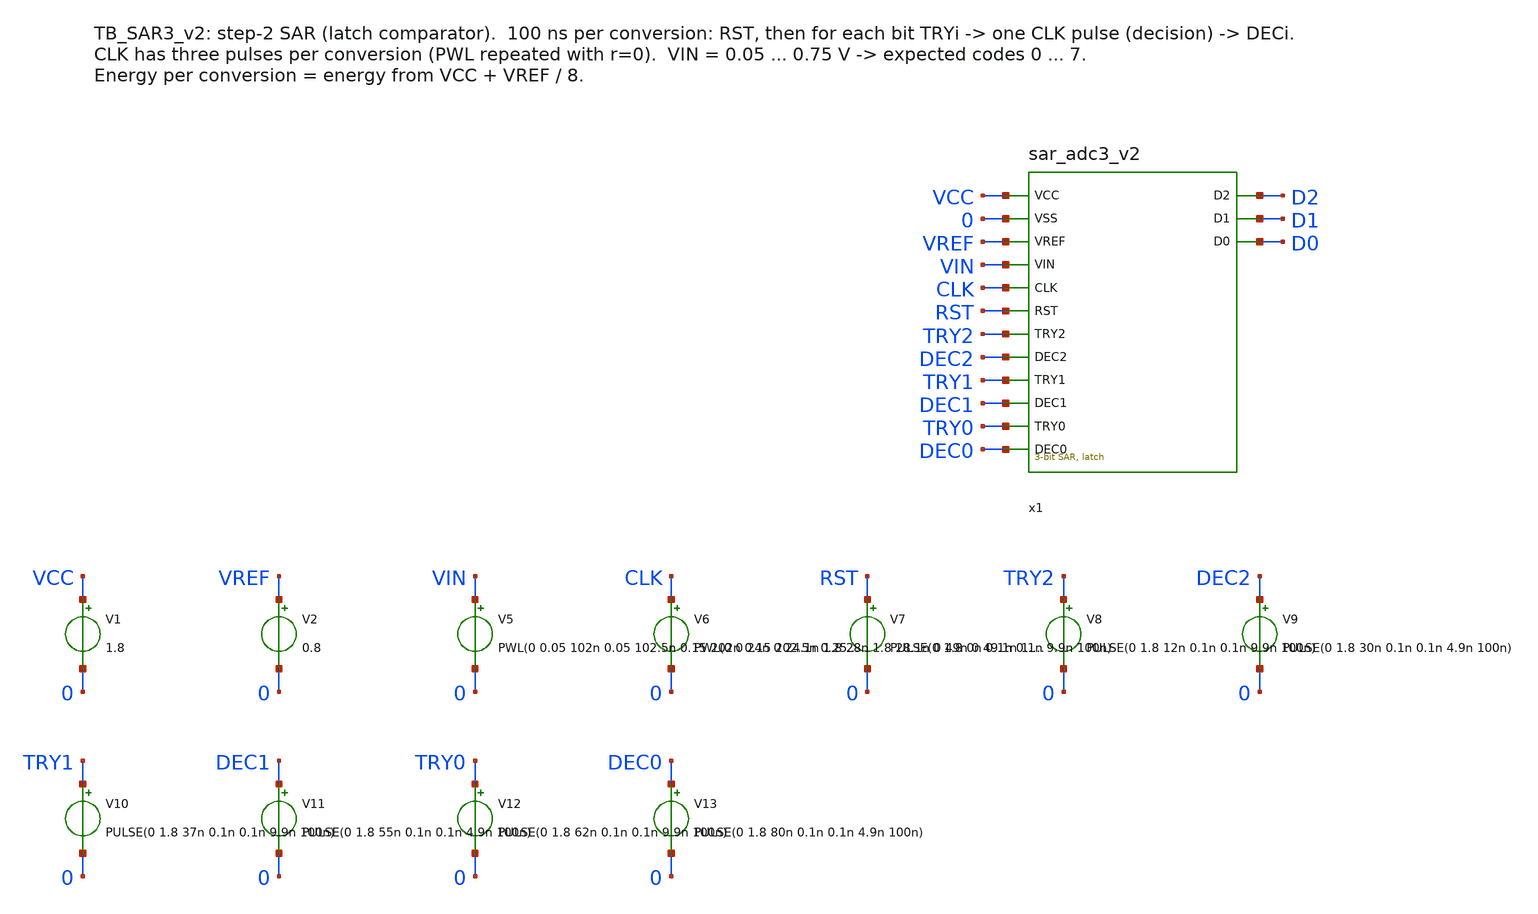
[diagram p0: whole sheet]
** sch_path: SAR_improved/TB_SAR3_v2.sch
**.subckt TB_SAR3_v2
x1 VCC 0 VREF VIN CLK RST TRY2 DEC2 TRY1 DEC1 TRY0 DEC0 D2 D1 D0 sar_adc3_v2
V1 VCC 0 1.8
V2 VREF 0 0.8
V5 VIN 0 PWL(0 0.05 102n 0.05 102.5n 0.15 202n 0.15 202.5n 0.25 302n 0.25 302.5n 0.35 402n 0.35
+ 402.5n 0.45 502n 0.45 502.5n 0.55 602n 0.55 602.5n 0.65 702n 0.65 702.5n 0.75)
V6 CLK 0 PWL(0 0 24n 0 24.1n 1.8 28n 1.8 28.1n 0 49n 0 49.1n 1.8 53n 1.8 53.1n 0 74n 0 74.1n 1.8 78n
+ 1.8 78.1n 0 100n 0) r=0
V7 RST 0 PULSE(0 1.8 0n 0.1n 0.1n 9.9n 100n)
V8 TRY2 0 PULSE(0 1.8 12n 0.1n 0.1n 9.9n 100n)
V9 DEC2 0 PULSE(0 1.8 30n 0.1n 0.1n 4.9n 100n)
V10 TRY1 0 PULSE(0 1.8 37n 0.1n 0.1n 9.9n 100n)
V11 DEC1 0 PULSE(0 1.8 55n 0.1n 0.1n 4.9n 100n)
V12 TRY0 0 PULSE(0 1.8 62n 0.1n 0.1n 9.9n 100n)
V13 DEC0 0 PULSE(0 1.8 80n 0.1n 0.1n 4.9n 100n)
**** begin user architecture code

.lib /home/ttuser/pdk/sky130A/libs.tech/combined/sky130.lib.spice tt
.option method=gear reltol=1e-4
.control
save all
tran 0.025n 800n
let code = 4*ceil((v(D2)-0.9)/10) + 2*ceil((v(D1)-0.9)/10) + ceil((v(D0)-0.9)/10)
meas tran code1 find code at=90n
meas tran code2 find code at=190n
meas tran code3 find code at=290n
meas tran code4 find code at=390n
meas tran code5 find code at=490n
meas tran code6 find code at=590n
meas tran code7 find code at=690n
meas tran code8 find code at=790n
let ptot = 1.8*(-i(V1)) + 0.8*(-i(V2))
meas tran etot integ ptot from=0 to=800n
let e_conv_pJ = etot/8*1e12
let p_uW = etot/800e-9*1e6
print e_conv_pJ p_uW
plot v(VIN) v(x1.REF)
plot v(CLK) v(x1.COM)+2
plot v(D2) v(D1)+2 v(D0)+4
plot code v(VIN)
.endc

**** end user architecture code
**.ends
.end
